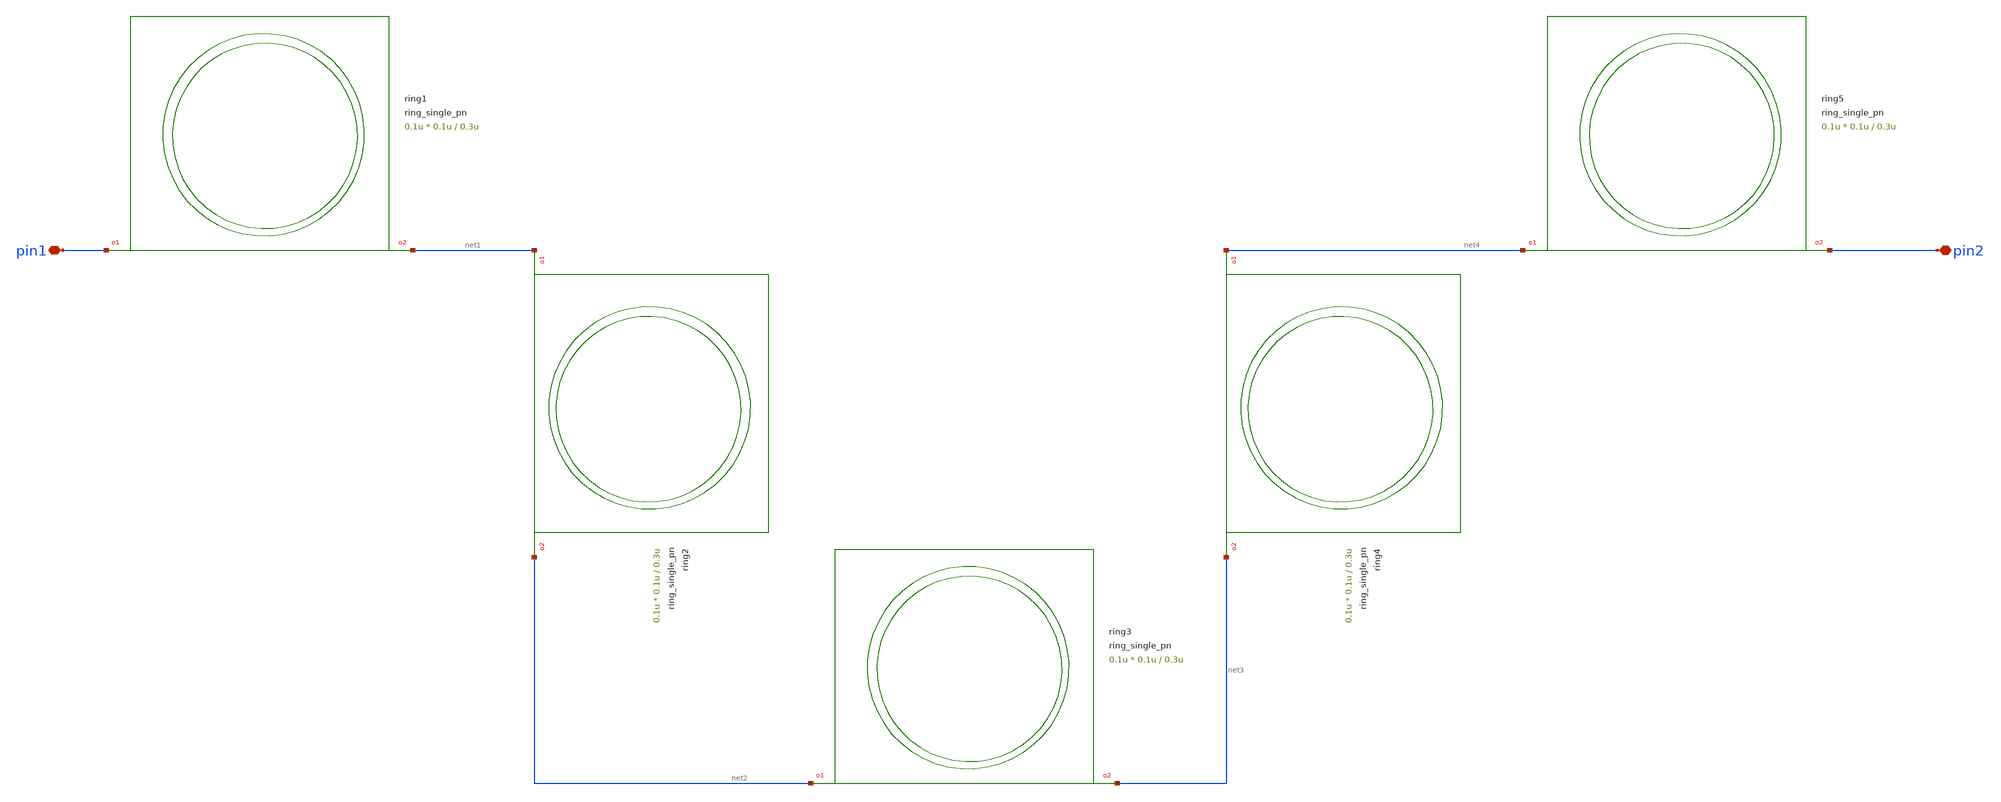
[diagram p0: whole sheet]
** sch_path: xschem/tests/test_sch/test_ring_single_pn.sch
* Copyright (c) 2024, Mabrains LLC
* Licensed under the GNU Lesser General Public License, Version 3.0 (the "License");
* you may not use this file except in compliance with the License.
* GNU Lesser General Public License
* Version 3, 29 June 2007
* This program is free software: you can redistribute it and/or modify
* it under the terms of the GNU Lesser General Public License as published
* by the Free Software Foundation, either version 3 of the License, or
* (at your option) any later version.
* This program is distributed in the hope that it will be useful,
* but WITHOUT ANY WARRANTY; without even the implied warranty of
* MERCHANTABILITY or FITNESS FOR A PARTICULAR PURPOSE.  See the
* GNU Lesser General Public License for more details.
* You should have received a copy of the GNU Lesser General Public License
* along with this program.  If not, see <https://www.gnu.org/licenses/>.
* SPDX-License-Identifier: LGPL-3.0
**.subckt test_ring_single_pn pin1 pin2
*.iopin pin1
*.iopin pin2
Pring1 pin1 net1 ring_single_pn gap=0.3u radius=5.0u doping_angle=250 length_x=0.1u length_y=0.1u
Pring3 net2 net3 ring_single_pn gap=0.3u radius=5.0u doping_angle=250 length_x=0.1u length_y=0.1u
Pring5 net4 pin2 ring_single_pn gap=0.3u radius=5.0u doping_angle=250 length_x=0.1u length_y=0.1u
Pring2 net1 net2 ring_single_pn gap=0.3u radius=5.0u doping_angle=250 length_x=0.1u length_y=0.1u
Pring4 net4 net3 ring_single_pn gap=0.3u radius=5.0u doping_angle=250 length_x=0.1u length_y=0.1u
**.ends
.end
